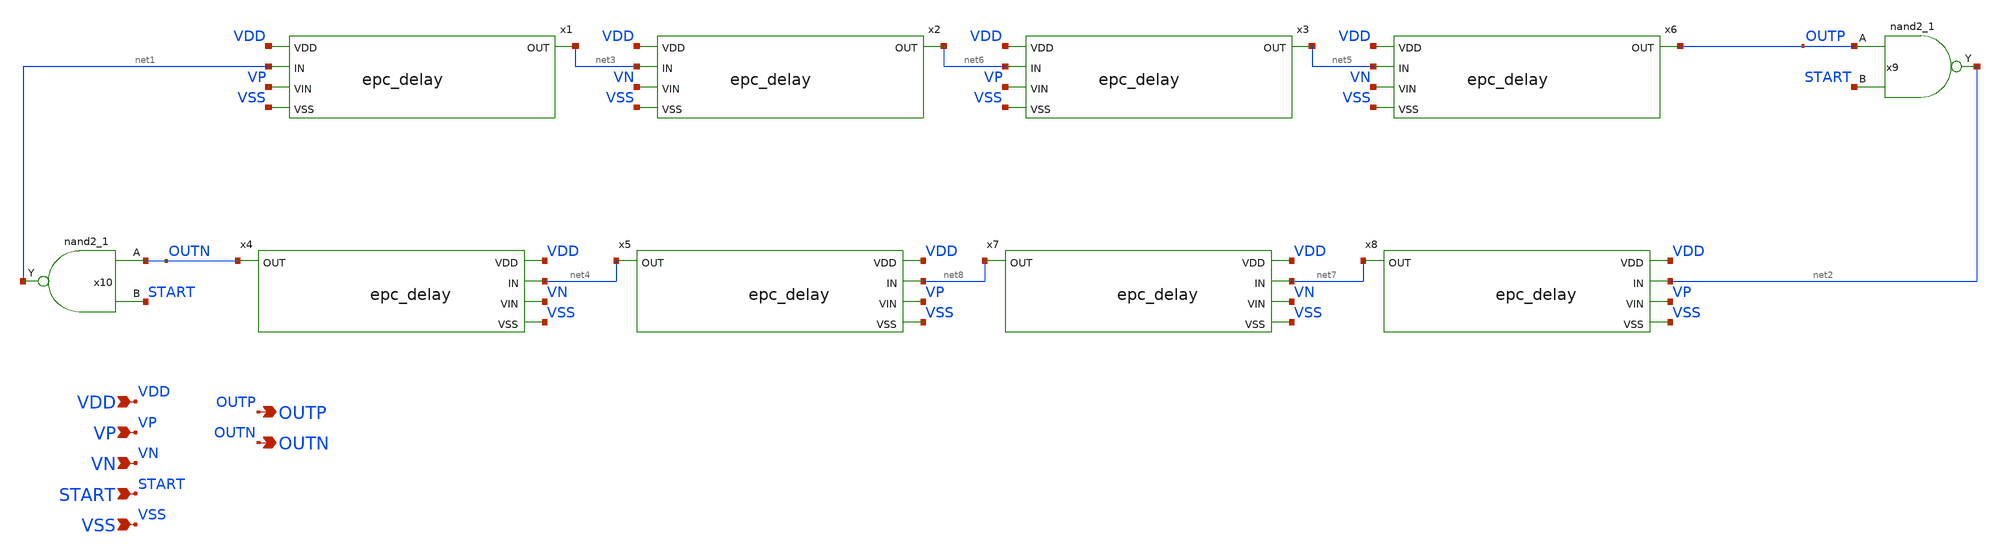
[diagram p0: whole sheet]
** sch_path: xschem/epc.sch
**.subckt epc VDD VP VN VSS OUTP START OUTN
*.ipin VDD
*.ipin VP
*.ipin VN
*.ipin VSS
*.opin OUTP
*.ipin START
*.opin OUTN
x9 OUTP START VSS VSS VDD VDD net2 sky130_fd_sc_hd__nand2_1
x10 OUTN START VSS VSS VDD VDD net1 sky130_fd_sc_hd__nand2_1
x1 VDD net1 net3 VP VSS epc_delay
x2 VDD net3 net6 VN VSS epc_delay
x4 VDD net4 OUTN VN VSS epc_delay
x5 VDD net8 net4 VP VSS epc_delay
x3 VDD net6 net5 VP VSS epc_delay
x6 VDD net5 OUTP VN VSS epc_delay
x7 VDD net7 net8 VN VSS epc_delay
x8 VDD net2 net7 VP VSS epc_delay
**.ends

* expanding   symbol:  epc_delay.sym # of pins=5
** sym_path: epc_delay.sym
** sch_path: epc_delay.sch
.subckt epc_delay VDD IN OUT VIN VSS
*.ipin VDD
*.ipin VIN
*.ipin IN
*.ipin VSS
*.opin OUT
.param W_N=0.5 L_N=0.5 W_P=1.0 L_P=0.5
XM1 net2 VIN VDD VDD sky130_fd_pr__pfet_01v8_lvt L=L_P W=W_P nf=1 ad='int((nf+1)/2) * W/nf * 0.29' as='int((nf+2)/2) * W/nf * 0.29'
+ pd='2*int((nf+1)/2) * (W/nf + 0.29)' ps='2*int((nf+2)/2) * (W/nf + 0.29)' nrd='0.29 / W' nrs='0.29 / W'
+ sa=0 sb=0 sd=0 mult=1 m=1
XM2 OUT IN net2 VDD sky130_fd_pr__pfet_01v8_lvt L=L_P W=W_P nf=1 ad='int((nf+1)/2) * W/nf * 0.29' as='int((nf+2)/2) * W/nf * 0.29'
+ pd='2*int((nf+1)/2) * (W/nf + 0.29)' ps='2*int((nf+2)/2) * (W/nf + 0.29)' nrd='0.29 / W' nrs='0.29 / W'
+ sa=0 sb=0 sd=0 mult=1 m=1
XM3 OUT IN net1 VSS sky130_fd_pr__nfet_01v8_lvt L=L_N W=W_N nf=1 ad='int((nf+1)/2) * W/nf * 0.29' as='int((nf+2)/2) * W/nf * 0.29'
+ pd='2*int((nf+1)/2) * (W/nf + 0.29)' ps='2*int((nf+2)/2) * (W/nf + 0.29)' nrd='0.29 / W' nrs='0.29 / W'
+ sa=0 sb=0 sd=0 mult=1 m=1
XM4 net1 VIN VSS VSS sky130_fd_pr__nfet_01v8_lvt L=L_N W=W_N nf=1 ad='int((nf+1)/2) * W/nf * 0.29' as='int((nf+2)/2) * W/nf * 0.29'
+ pd='2*int((nf+1)/2) * (W/nf + 0.29)' ps='2*int((nf+2)/2) * (W/nf + 0.29)' nrd='0.29 / W' nrs='0.29 / W'
+ sa=0 sb=0 sd=0 mult=1 m=1
.ends

.end
